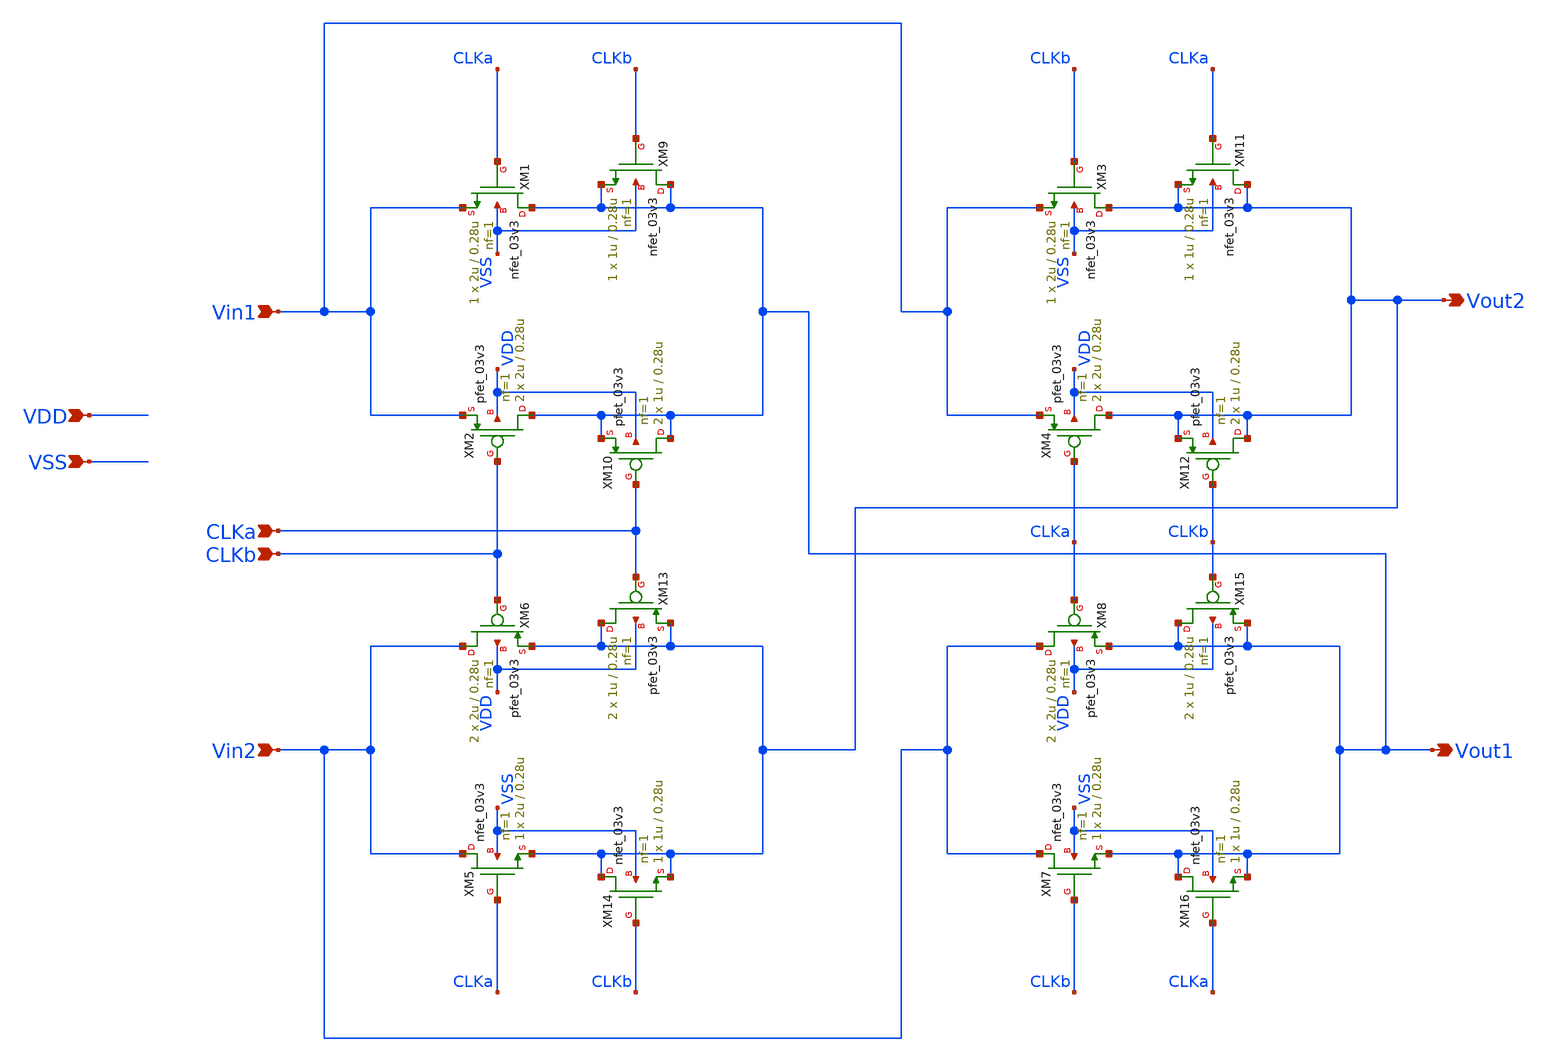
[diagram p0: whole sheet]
** sch_path: designs/libs/core_ina/ina_chopper/ina_chopper.sch
**.subckt ina_chopper Vin1 Vin2 CLKb Vout2 CLKa Vout1 VDD VSS
*.ipin Vin1
*.ipin Vin2
*.ipin CLKb
*.opin Vout2
*.ipin CLKa
*.opin Vout1
*.ipin VDD
*.ipin VSS
XM1 Vout1 CLKa Vin1 VSS nfet_03v3 L=0.28u W=2u nf=1 ad='int((nf+1)/2) * W/nf * 0.18u' as='int((nf+2)/2) * W/nf * 0.18u'
+ pd='2*int((nf+1)/2) * (W/nf + 0.18u)' ps='2*int((nf+2)/2) * (W/nf + 0.18u)' nrd='0.18u / W' nrs='0.18u / W'
+ sa=0 sb=0 sd=0 m=1
XM2 Vout1 CLKb Vin1 VDD pfet_03v3 L=0.28u W=2u nf=1 ad='int((nf+1)/2) * W/nf * 0.18u' as='int((nf+2)/2) * W/nf * 0.18u'
+ pd='2*int((nf+1)/2) * (W/nf + 0.18u)' ps='2*int((nf+2)/2) * (W/nf + 0.18u)' nrd='0.18u / W' nrs='0.18u / W'
+ sa=0 sb=0 sd=0 m=2
XM3 Vout2 CLKb Vin1 VSS nfet_03v3 L=0.28u W=2u nf=1 ad='int((nf+1)/2) * W/nf * 0.18u' as='int((nf+2)/2) * W/nf * 0.18u'
+ pd='2*int((nf+1)/2) * (W/nf + 0.18u)' ps='2*int((nf+2)/2) * (W/nf + 0.18u)' nrd='0.18u / W' nrs='0.18u / W'
+ sa=0 sb=0 sd=0 m=1
XM4 Vout2 CLKa Vin1 VDD pfet_03v3 L=0.28u W=2u nf=1 ad='int((nf+1)/2) * W/nf * 0.18u' as='int((nf+2)/2) * W/nf * 0.18u'
+ pd='2*int((nf+1)/2) * (W/nf + 0.18u)' ps='2*int((nf+2)/2) * (W/nf + 0.18u)' nrd='0.18u / W' nrs='0.18u / W'
+ sa=0 sb=0 sd=0 m=2
XM5 Vin2 CLKa Vout2 VSS nfet_03v3 L=0.28u W=2u nf=1 ad='int((nf+1)/2) * W/nf * 0.18u' as='int((nf+2)/2) * W/nf * 0.18u'
+ pd='2*int((nf+1)/2) * (W/nf + 0.18u)' ps='2*int((nf+2)/2) * (W/nf + 0.18u)' nrd='0.18u / W' nrs='0.18u / W'
+ sa=0 sb=0 sd=0 m=1
XM6 Vin2 CLKb Vout2 VDD pfet_03v3 L=0.28u W=2u nf=1 ad='int((nf+1)/2) * W/nf * 0.18u' as='int((nf+2)/2) * W/nf * 0.18u'
+ pd='2*int((nf+1)/2) * (W/nf + 0.18u)' ps='2*int((nf+2)/2) * (W/nf + 0.18u)' nrd='0.18u / W' nrs='0.18u / W'
+ sa=0 sb=0 sd=0 m=2
XM7 Vin2 CLKb Vout1 VSS nfet_03v3 L=0.28u W=2u nf=1 ad='int((nf+1)/2) * W/nf * 0.18u' as='int((nf+2)/2) * W/nf * 0.18u'
+ pd='2*int((nf+1)/2) * (W/nf + 0.18u)' ps='2*int((nf+2)/2) * (W/nf + 0.18u)' nrd='0.18u / W' nrs='0.18u / W'
+ sa=0 sb=0 sd=0 m=1
XM8 Vin2 CLKa Vout1 VDD pfet_03v3 L=0.28u W=2u nf=1 ad='int((nf+1)/2) * W/nf * 0.18u' as='int((nf+2)/2) * W/nf * 0.18u'
+ pd='2*int((nf+1)/2) * (W/nf + 0.18u)' ps='2*int((nf+2)/2) * (W/nf + 0.18u)' nrd='0.18u / W' nrs='0.18u / W'
+ sa=0 sb=0 sd=0 m=2
XM9 Vout1 CLKb Vout1 VSS nfet_03v3 L=0.28u W=1u nf=1 ad='int((nf+1)/2) * W/nf * 0.18u' as='int((nf+2)/2) * W/nf * 0.18u'
+ pd='2*int((nf+1)/2) * (W/nf + 0.18u)' ps='2*int((nf+2)/2) * (W/nf + 0.18u)' nrd='0.18u / W' nrs='0.18u / W'
+ sa=0 sb=0 sd=0 m=1
XM10 Vout1 CLKa Vout1 VDD pfet_03v3 L=0.28u W=1u nf=1 ad='int((nf+1)/2) * W/nf * 0.18u' as='int((nf+2)/2) * W/nf * 0.18u'
+ pd='2*int((nf+1)/2) * (W/nf + 0.18u)' ps='2*int((nf+2)/2) * (W/nf + 0.18u)' nrd='0.18u / W' nrs='0.18u / W'
+ sa=0 sb=0 sd=0 m=2
XM11 Vout2 CLKa Vout2 VSS nfet_03v3 L=0.28u W=1u nf=1 ad='int((nf+1)/2) * W/nf * 0.18u' as='int((nf+2)/2) * W/nf * 0.18u'
+ pd='2*int((nf+1)/2) * (W/nf + 0.18u)' ps='2*int((nf+2)/2) * (W/nf + 0.18u)' nrd='0.18u / W' nrs='0.18u / W'
+ sa=0 sb=0 sd=0 m=1
XM12 Vout2 CLKb Vout2 VDD pfet_03v3 L=0.28u W=1u nf=1 ad='int((nf+1)/2) * W/nf * 0.18u' as='int((nf+2)/2) * W/nf * 0.18u'
+ pd='2*int((nf+1)/2) * (W/nf + 0.18u)' ps='2*int((nf+2)/2) * (W/nf + 0.18u)' nrd='0.18u / W' nrs='0.18u / W'
+ sa=0 sb=0 sd=0 m=2
XM13 Vout2 CLKa Vout2 VDD pfet_03v3 L=0.28u W=1u nf=1 ad='int((nf+1)/2) * W/nf * 0.18u' as='int((nf+2)/2) * W/nf * 0.18u'
+ pd='2*int((nf+1)/2) * (W/nf + 0.18u)' ps='2*int((nf+2)/2) * (W/nf + 0.18u)' nrd='0.18u / W' nrs='0.18u / W'
+ sa=0 sb=0 sd=0 m=2
XM14 Vout2 CLKb Vout2 VSS nfet_03v3 L=0.28u W=1u nf=1 ad='int((nf+1)/2) * W/nf * 0.18u' as='int((nf+2)/2) * W/nf * 0.18u'
+ pd='2*int((nf+1)/2) * (W/nf + 0.18u)' ps='2*int((nf+2)/2) * (W/nf + 0.18u)' nrd='0.18u / W' nrs='0.18u / W'
+ sa=0 sb=0 sd=0 m=1
XM15 Vout1 CLKb Vout1 VDD pfet_03v3 L=0.28u W=1u nf=1 ad='int((nf+1)/2) * W/nf * 0.18u' as='int((nf+2)/2) * W/nf * 0.18u'
+ pd='2*int((nf+1)/2) * (W/nf + 0.18u)' ps='2*int((nf+2)/2) * (W/nf + 0.18u)' nrd='0.18u / W' nrs='0.18u / W'
+ sa=0 sb=0 sd=0 m=2
XM16 Vout1 CLKa Vout1 VSS nfet_03v3 L=0.28u W=1u nf=1 ad='int((nf+1)/2) * W/nf * 0.18u' as='int((nf+2)/2) * W/nf * 0.18u'
+ pd='2*int((nf+1)/2) * (W/nf + 0.18u)' ps='2*int((nf+2)/2) * (W/nf + 0.18u)' nrd='0.18u / W' nrs='0.18u / W'
+ sa=0 sb=0 sd=0 m=1
**.ends
.end
